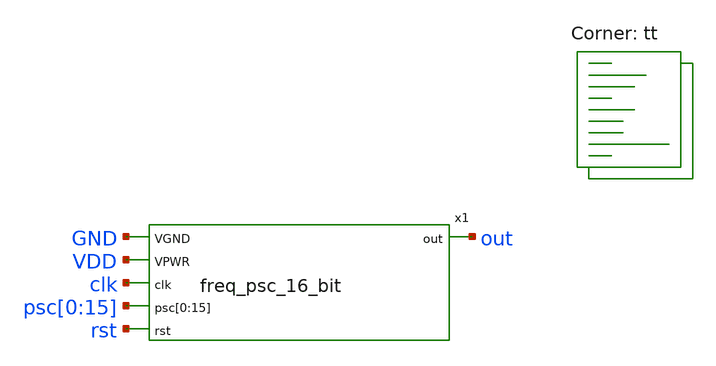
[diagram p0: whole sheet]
** sch_path: xschem/freq_psc_16_bit-tb.sch
**.subckt freq_psc_16_bit-tb
x1 GND VDD clk out psc[0] psc[1] psc[2] psc[3] psc[4] psc[5] psc[6] psc[7] psc[8] psc[9] psc[10]
+ psc[11] psc[12] psc[13] psc[14] psc[15] rst freq_psc_16_bit
**** begin user architecture code



  .include ~/sky130_projects/sky130_its_biomedical_chip_research_2024/spice/freq_psc_16_bit.spice
  .param max_freq=100e6 period={1/max_freq} time_high={period/2}
  .param delay_vin1={time_high} delay_vin2={time_high*1.5}

  .option wnflag=1
  .option safecurrents

  Vvdd VDD GND dc 1.8
  Vrst rst GND pulse(0 1.8 {delay_vin1*20} 1p 1p {time_high*20} {period*50})
  Vin1 clk GND pulse(0 1.8 {delay_vin1} 1p 1p {time_high} {period})

  Vpsc0   psc[0]  gnd dc 0
  Vpsc1   psc[1]  gnd dc 0
  Vpsc2   psc[2]  gnd dc 1
  Vpsc3   psc[3]  gnd dc 0
  Vpsc4   psc[4]  gnd dc 0
  Vpsc5   psc[5]  gnd dc 0
  Vpsc6   psc[6]  gnd dc 0
  Vpsc7   psc[7]  gnd dc 0
  Vpsc8   psc[8]  gnd dc 0
  Vpsc9   psc[9]  gnd dc 0
  Vpsc10  psc[10] gnd dc 0
  Vpsc11  psc[11] gnd dc 0
  Vpsc12  psc[12] gnd dc 0
  Vpsc13  psc[13] gnd dc 0
  Vpsc14  psc[14] gnd dc 0
  Vpsc15  psc[15] gnd dc 0

  .control
     reset
     save out clk psc[0] psc[1] psc[2] psc[3] psc[4] psc[5]
     +psc[6] psc[7] psc[8] psc[9] psc[10] psc[11] psc[12] psc[13]
     +psc[14] psc[15] rst
     tran 0.01n 500n uic
     remzerovec
     write freq_psc_16_bit-tb.raw
    quit 0
  .endc



 .lib $::SKYWATER_MODELS/sky130.lib.spice tt
.include $::SKYWATER_STDCELLS/sky130_fd_sc_hd.spice
.include $::SKYWATER_STDCELLS/sky130_ef_sc_hd__decap_12.spice
.include $::SKYWATER_STDCELLS/sky130_ef_sc_hd__fill_4.spice
.include $::SKYWATER_STDCELLS/sky130_ef_sc_hd__fill_8.spice
.include $::SKYWATER_STDCELLS/sky130_ef_sc_hd__fill_12.spice
.param mc_mm_switch = 0
.param mc_pr_switch = 0

**** end user architecture code
**.ends
.end
